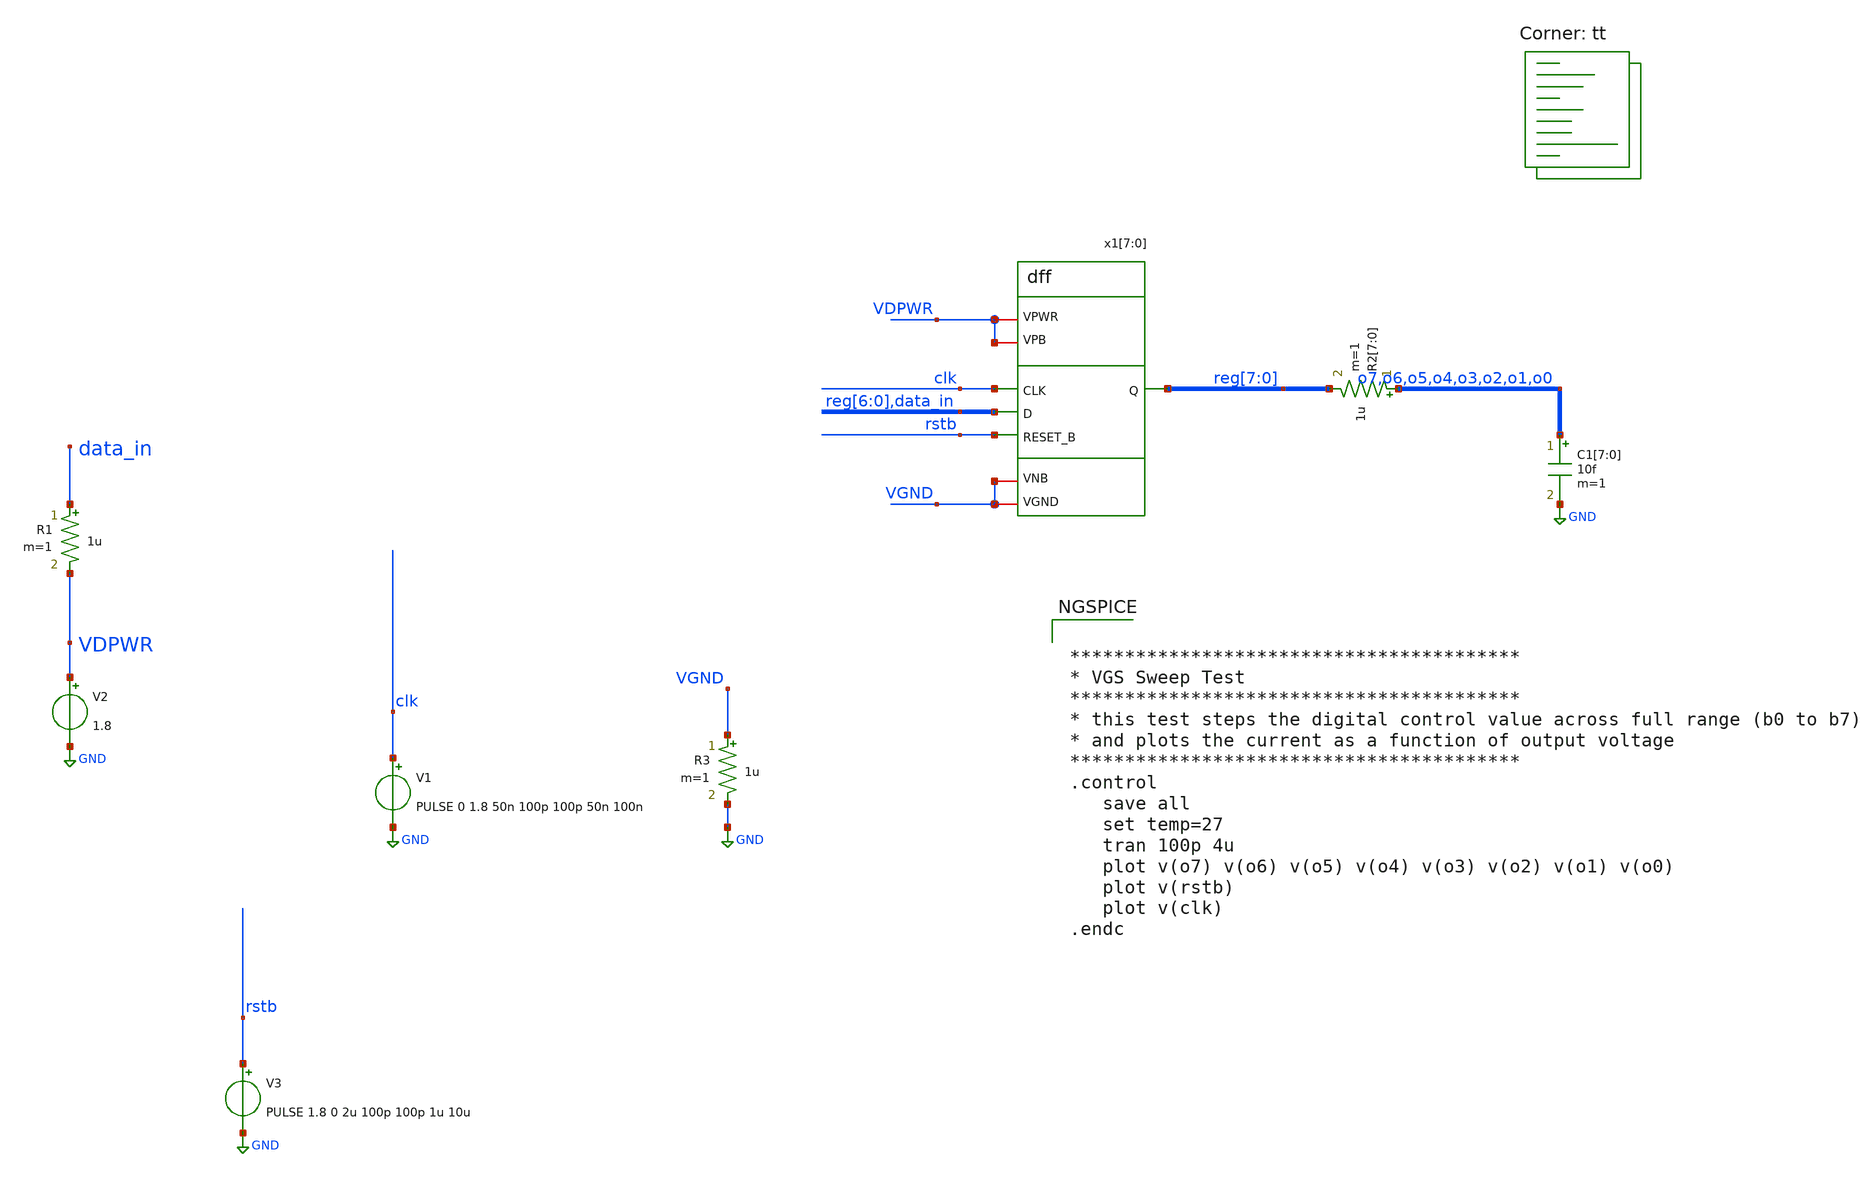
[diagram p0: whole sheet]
** sch_path: xschem/tb_temp.sch
**.subckt tb_temp
V1 clk GND PULSE 0 1.8 50n 100p 100p 50n 100n
x1[7] clk reg[6] rstb VGND VGND VDPWR VDPWR reg[7] dff
x1[6] clk reg[5] rstb VGND VGND VDPWR VDPWR reg[6] dff
x1[5] clk reg[4] rstb VGND VGND VDPWR VDPWR reg[5] dff
x1[4] clk reg[3] rstb VGND VGND VDPWR VDPWR reg[4] dff
x1[3] clk reg[2] rstb VGND VGND VDPWR VDPWR reg[3] dff
x1[2] clk reg[1] rstb VGND VGND VDPWR VDPWR reg[2] dff
x1[1] clk reg[0] rstb VGND VGND VDPWR VDPWR reg[1] dff
x1[0] clk data_in rstb VGND VGND VDPWR VDPWR reg[0] dff
V2 VDPWR GND 1.8
R1 data_in VDPWR 1u m=1
R3 VGND GND 1u m=1
V3 rstb GND PULSE 1.8 0 2u 100p 100p 1u 10u
R2[7] o7 reg[7] 1u m=1
R2[6] o6 reg[6] 1u m=1
R2[5] o5 reg[5] 1u m=1
R2[4] o4 reg[4] 1u m=1
R2[3] o3 reg[3] 1u m=1
R2[2] o2 reg[2] 1u m=1
R2[1] o1 reg[1] 1u m=1
R2[0] o0 reg[0] 1u m=1
C1[7] o7 GND 10f m=1
C1[6] o6 GND 10f m=1
C1[5] o5 GND 10f m=1
C1[4] o4 GND 10f m=1
C1[3] o3 GND 10f m=1
C1[2] o2 GND 10f m=1
C1[1] o1 GND 10f m=1
C1[0] o0 GND 10f m=1
**** begin user architecture code
.lib $::SKYWATER_MODELS/sky130.lib.spice tt


*****************************************
* VGS Sweep Test
*****************************************
* this test steps the digital control value across full range (b0 to b7)
* and plots the current as a function of output voltage
*****************************************
.control
   save all
   set temp=27
   tran 100p 4u
   plot v(o7) v(o6) v(o5) v(o4) v(o3) v(o2) v(o1) v(o0)
   plot v(rstb)
   plot v(clk)
.endc


**** end user architecture code
**.ends

* expanding   symbol:  dff.sym # of pins=8
** sym_path: xschem/dff.sym
** sch_path: xschem/dff.sch
.subckt dff CLK D RESET_B VGND VNB VPB VPWR Q
*.ipin CLK
*.ipin D
*.ipin RESET_B
*.iopin VGND
*.iopin VNB
*.iopin VPB
*.iopin VPWR
*.opin Q
**** begin user architecture code


X0 a_1270_413# a_1283_21# VPWR VPB sky130_fd_pr__pfet_01v8_hvt w=420000u l=150000u
X1 VPWR a_543_47# a_761_289# VPB sky130_fd_pr__pfet_01v8_hvt w=840000u l=150000u
X2 VGND a_543_47# a_761_289# VNB sky130_fd_pr__nfet_01v8 w=640000u l=150000u
X3 VGND D a_448_47# VNB sky130_fd_pr__nfet_01v8 w=420000u l=150000u
X4 a_1108_47# a_193_47# a_1270_413# VPB sky130_fd_pr__pfet_01v8_hvt w=420000u l=150000u
X5 VGND a_1283_21# Q VNB sky130_fd_pr__nfet_01v8 w=650000u l=150000u
X6 a_1217_47# a_1283_21# VGND VNB sky130_fd_pr__nfet_01v8 w=420000u l=150000u
X7 a_448_47# a_27_47# a_543_47# VNB sky130_fd_pr__nfet_01v8 w=360000u l=150000u
X8 a_448_47# a_193_47# a_543_47# VPB sky130_fd_pr__pfet_01v8_hvt w=420000u l=150000u
X9 a_543_47# a_193_47# a_639_47# VNB sky130_fd_pr__nfet_01v8 w=360000u l=150000u
X10 a_1108_47# a_27_47# a_1217_47# VNB sky130_fd_pr__nfet_01v8 w=360000u l=150000u
X11 a_1462_47# a_1108_47# a_1283_21# VNB sky130_fd_pr__nfet_01v8 w=420000u l=150000u
X12 a_543_47# a_27_47# a_651_413# VPB sky130_fd_pr__pfet_01v8_hvt w=420000u l=150000u
X13 a_805_47# RESET_B VGND VNB sky130_fd_pr__nfet_01v8 w=420000u l=150000u
X14 a_761_289# a_193_47# a_1108_47# VNB sky130_fd_pr__nfet_01v8 w=360000u l=150000u
X15 VPWR RESET_B a_651_413# VPB sky130_fd_pr__pfet_01v8_hvt w=420000u l=150000u
X16 VGND a_27_47# a_193_47# VNB sky130_fd_pr__nfet_01v8 w=420000u l=150000u
X17 a_27_47# CLK VGND VNB sky130_fd_pr__nfet_01v8 w=420000u l=150000u
X18 a_27_47# CLK VPWR VPB sky130_fd_pr__pfet_01v8_hvt w=640000u l=150000u
X19 VPWR a_1283_21# Q VPB sky130_fd_pr__pfet_01v8_hvt w=1e+06u l=150000u
X20 VPWR a_27_47# a_193_47# VPB sky130_fd_pr__pfet_01v8_hvt w=640000u l=150000u
X21 a_1283_21# a_1108_47# VPWR VPB sky130_fd_pr__pfet_01v8_hvt w=420000u l=150000u
X22 VGND RESET_B a_1462_47# VNB sky130_fd_pr__nfet_01v8 w=420000u l=150000u
X23 VPWR D a_448_47# VPB sky130_fd_pr__pfet_01v8_hvt w=420000u l=150000u
X24 a_651_413# a_761_289# VPWR VPB sky130_fd_pr__pfet_01v8_hvt w=420000u l=150000u
X25 a_761_289# a_27_47# a_1108_47# VPB sky130_fd_pr__pfet_01v8_hvt w=420000u l=150000u
X26 VPWR RESET_B a_1283_21# VPB sky130_fd_pr__pfet_01v8_hvt w=420000u l=150000u
X27 a_639_47# a_761_289# a_805_47# VNB sky130_fd_pr__nfet_01v8 w=420000u l=150000u


**** end user architecture code
**** begin user architecture code


**** end user architecture code
.ends

.GLOBAL GND
.end
